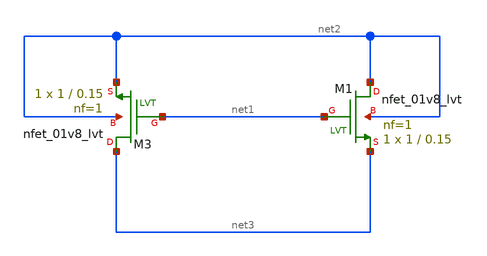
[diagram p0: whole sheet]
** sch_path: xschem/untitled-7.sch
**.subckt untitled-7
XM3 net3 net1 net2 net2 sky130_fd_pr__nfet_01v8_lvt L=0.15 W=1 nf=1 ad='int((1 + 1)/2) * 1 / 1 * 0.29'
+ as='int((1 + 2)/2) * 1 / 1 * 0.29' pd='2*int((1 + 1)/2) * (1 / 1 + 0.29)' ps='2*int((1 + 2)/2) * (1 / 1 + 0.29)'
+ nrd='0.29 / 1 ' nrs='0.29 / 1 ' sa=0 sb=0 sd=0 mult=1 m=1
XM1 net2 net1 net3 net2 sky130_fd_pr__nfet_01v8_lvt L=0.15 W=1 nf=1 ad='int((1 + 1)/2) * 1 / 1 * 0.29'
+ as='int((1 + 2)/2) * 1 / 1 * 0.29' pd='2*int((1 + 1)/2) * (1 / 1 + 0.29)' ps='2*int((1 + 2)/2) * (1 / 1 + 0.29)'
+ nrd='0.29 / 1 ' nrs='0.29 / 1 ' sa=0 sb=0 sd=0 mult=1 m=1
**.ends
.end
